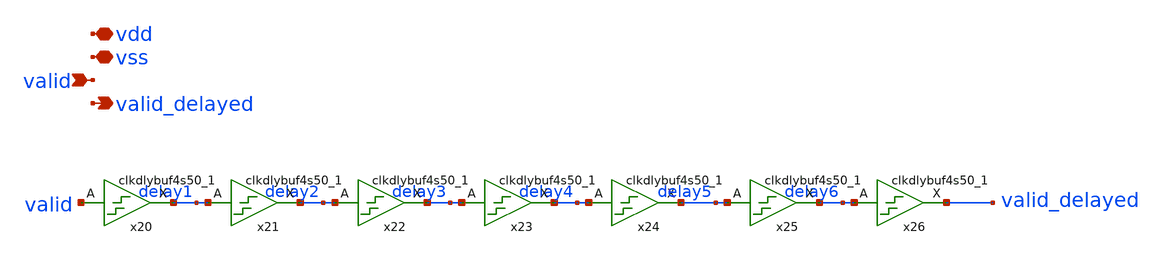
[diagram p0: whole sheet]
** sch_path: xschem/sar-adc/delay_control.sch
**.subckt delay_control valid vdd vss valid_delayed
*.ipin valid
*.iopin vdd
*.iopin vss
*.opin valid_delayed
x20 valid vss vss vdd vdd delay1 sky130_fd_sc_hd__clkdlybuf4s50_1
x21 delay1 vss vss vdd vdd delay2 sky130_fd_sc_hd__clkdlybuf4s50_1
x22 delay2 vss vss vdd vdd delay3 sky130_fd_sc_hd__clkdlybuf4s50_1
x23 delay3 vss vss vdd vdd delay4 sky130_fd_sc_hd__clkdlybuf4s50_1
x24 delay4 vss vss vdd vdd delay5 sky130_fd_sc_hd__clkdlybuf4s50_1
x25 delay5 vss vss vdd vdd delay6 sky130_fd_sc_hd__clkdlybuf4s50_1
x26 delay6 vss vss vdd vdd valid_delayed sky130_fd_sc_hd__clkdlybuf4s50_1
**.ends
.end
